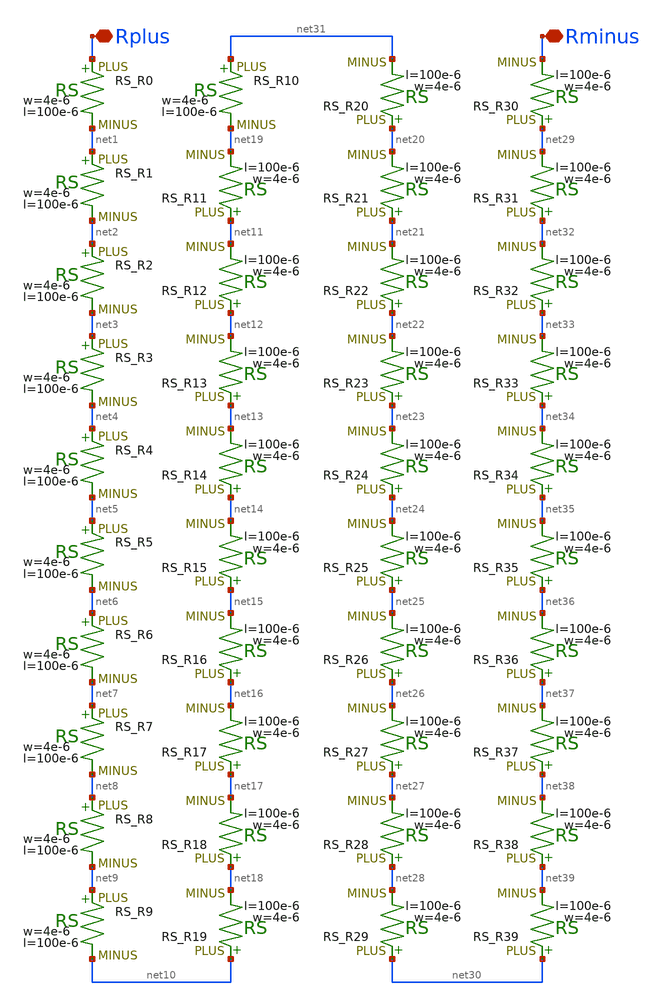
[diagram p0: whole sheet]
** sch_path: Vol.2/files/05/xschem/Vref_resistor40.sch
**.subckt Vref_resistor40 Rplus Rminus
*.iopin Rplus
*.iopin Rminus
XR0 Rplus net1 F_RS w=4e-6 R=1 l=100e-6 tc1=0 tc2=0
XR1 net1 net2 F_RS w=4e-6 R=1 l=100e-6 tc1=0 tc2=0
XR2 net2 net3 F_RS w=4e-6 R=1 l=100e-6 tc1=0 tc2=0
XR3 net3 net4 F_RS w=4e-6 R=1 l=100e-6 tc1=0 tc2=0
XR4 net4 net5 F_RS w=4e-6 R=1 l=100e-6 tc1=0 tc2=0
XR5 net5 net6 F_RS w=4e-6 R=1 l=100e-6 tc1=0 tc2=0
XR6 net6 net7 F_RS w=4e-6 R=1 l=100e-6 tc1=0 tc2=0
XR7 net7 net8 F_RS w=4e-6 R=1 l=100e-6 tc1=0 tc2=0
XR8 net8 net9 F_RS w=4e-6 R=1 l=100e-6 tc1=0 tc2=0
XR9 net9 net10 F_RS w=4e-6 R=1 l=100e-6 tc1=0 tc2=0
XR10 net31 net19 F_RS w=4e-6 R=1 l=100e-6 tc1=0 tc2=0
XR11 net11 net19 F_RS w=4e-6 R=1 l=100e-6 tc1=0 tc2=0
XR12 net12 net11 F_RS w=4e-6 R=1 l=100e-6 tc1=0 tc2=0
XR13 net13 net12 F_RS w=4e-6 R=1 l=100e-6 tc1=0 tc2=0
XR14 net14 net13 F_RS w=4e-6 R=1 l=100e-6 tc1=0 tc2=0
XR15 net15 net14 F_RS w=4e-6 R=1 l=100e-6 tc1=0 tc2=0
XR16 net16 net15 F_RS w=4e-6 R=1 l=100e-6 tc1=0 tc2=0
XR17 net17 net16 F_RS w=4e-6 R=1 l=100e-6 tc1=0 tc2=0
XR18 net18 net17 F_RS w=4e-6 R=1 l=100e-6 tc1=0 tc2=0
XR19 net10 net18 F_RS w=4e-6 R=1 l=100e-6 tc1=0 tc2=0
XR20 net20 net31 F_RS w=4e-6 R=1 l=100e-6 tc1=0 tc2=0
XR21 net21 net20 F_RS w=4e-6 R=1 l=100e-6 tc1=0 tc2=0
XR22 net22 net21 F_RS w=4e-6 R=1 l=100e-6 tc1=0 tc2=0
XR23 net23 net22 F_RS w=4e-6 R=1 l=100e-6 tc1=0 tc2=0
XR24 net24 net23 F_RS w=4e-6 R=1 l=100e-6 tc1=0 tc2=0
XR25 net25 net24 F_RS w=4e-6 R=1 l=100e-6 tc1=0 tc2=0
XR26 net26 net25 F_RS w=4e-6 R=1 l=100e-6 tc1=0 tc2=0
XR27 net27 net26 F_RS w=4e-6 R=1 l=100e-6 tc1=0 tc2=0
XR28 net28 net27 F_RS w=4e-6 R=1 l=100e-6 tc1=0 tc2=0
XR29 net30 net28 F_RS w=4e-6 R=1 l=100e-6 tc1=0 tc2=0
XR30 net29 Rminus F_RS w=4e-6 R=1 l=100e-6 tc1=0 tc2=0
XR31 net32 net29 F_RS w=4e-6 R=1 l=100e-6 tc1=0 tc2=0
XR32 net33 net32 F_RS w=4e-6 R=1 l=100e-6 tc1=0 tc2=0
XR33 net34 net33 F_RS w=4e-6 R=1 l=100e-6 tc1=0 tc2=0
XR34 net35 net34 F_RS w=4e-6 R=1 l=100e-6 tc1=0 tc2=0
XR35 net36 net35 F_RS w=4e-6 R=1 l=100e-6 tc1=0 tc2=0
XR36 net37 net36 F_RS w=4e-6 R=1 l=100e-6 tc1=0 tc2=0
XR37 net38 net37 F_RS w=4e-6 R=1 l=100e-6 tc1=0 tc2=0
XR38 net39 net38 F_RS w=4e-6 R=1 l=100e-6 tc1=0 tc2=0
XR39 net30 net39 F_RS w=4e-6 R=1 l=100e-6 tc1=0 tc2=0
**.ends
.end
